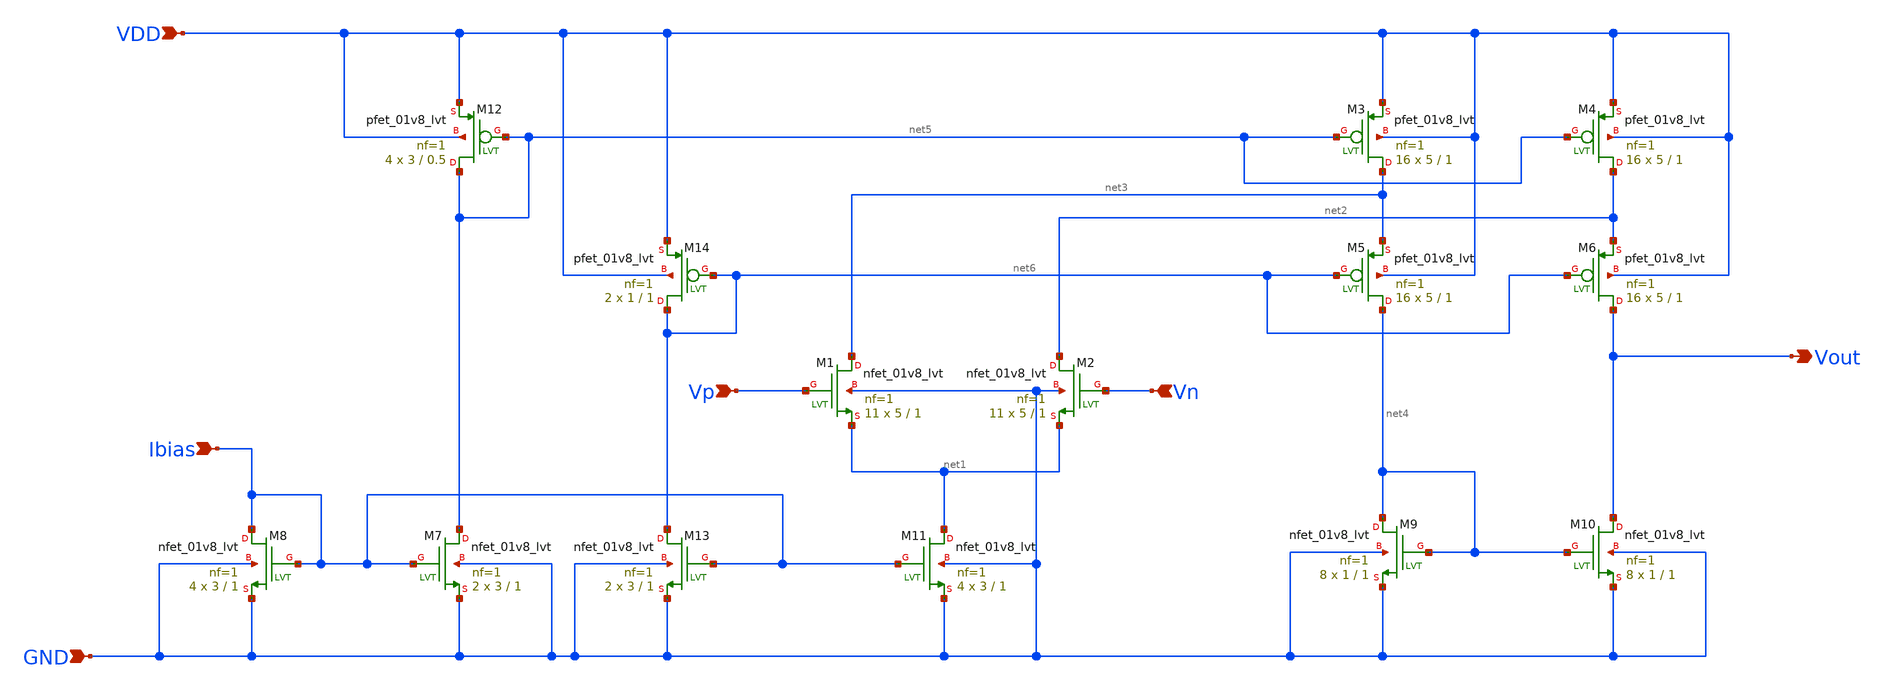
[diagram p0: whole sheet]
** sch_path: Analog_blocks/Analog_Blocks/OTA/Schematic/Folded_Cascode_OTA/Transistor1.8v/Folded_Cascode_OTA.sch
**.subckt Folded_Cascode_OTA VDD GND Vp Vn Vout Ibias
*.ipin VDD
*.ipin GND
*.ipin Vp
*.ipin Vn
*.opin Vout
*.ipin Ibias
XM1 net3 Vp net1 GND sky130_fd_pr__nfet_01v8_lvt L=1 W=5 nf=1 ad='int((nf+1)/2) * W/nf * 0.29' as='int((nf+2)/2) * W/nf * 0.29'
+ pd='2*int((nf+1)/2) * (W/nf + 0.29)' ps='2*int((nf+2)/2) * (W/nf + 0.29)' nrd='0.29 / W' nrs='0.29 / W'
+ sa=0 sb=0 sd=0 mult=11 m=11
XM2 net2 Vn net1 GND sky130_fd_pr__nfet_01v8_lvt L=1 W=5 nf=1 ad='int((nf+1)/2) * W/nf * 0.29' as='int((nf+2)/2) * W/nf * 0.29'
+ pd='2*int((nf+1)/2) * (W/nf + 0.29)' ps='2*int((nf+2)/2) * (W/nf + 0.29)' nrd='0.29 / W' nrs='0.29 / W'
+ sa=0 sb=0 sd=0 mult=11 m=11
XM3 net3 net5 VDD VDD sky130_fd_pr__pfet_01v8_lvt L=1 W=5 nf=1 ad='int((nf+1)/2) * W/nf * 0.29' as='int((nf+2)/2) * W/nf * 0.29'
+ pd='2*int((nf+1)/2) * (W/nf + 0.29)' ps='2*int((nf+2)/2) * (W/nf + 0.29)' nrd='0.29 / W' nrs='0.29 / W'
+ sa=0 sb=0 sd=0 mult=16 m=16
XM9 net4 net4 GND GND sky130_fd_pr__nfet_01v8_lvt L=1 W=1 nf=1 ad='int((nf+1)/2) * W/nf * 0.29' as='int((nf+2)/2) * W/nf * 0.29'
+ pd='2*int((nf+1)/2) * (W/nf + 0.29)' ps='2*int((nf+2)/2) * (W/nf + 0.29)' nrd='0.29 / W' nrs='0.29 / W'
+ sa=0 sb=0 sd=0 mult=8 m=8
XM10 Vout net4 GND GND sky130_fd_pr__nfet_01v8_lvt L=1 W=1 nf=1 ad='int((nf+1)/2) * W/nf * 0.29' as='int((nf+2)/2) * W/nf * 0.29'
+ pd='2*int((nf+1)/2) * (W/nf + 0.29)' ps='2*int((nf+2)/2) * (W/nf + 0.29)' nrd='0.29 / W' nrs='0.29 / W'
+ sa=0 sb=0 sd=0 mult=8 m=8
XM11 net1 Ibias GND GND sky130_fd_pr__nfet_01v8_lvt L=1 W=3 nf=1 ad='int((nf+1)/2) * W/nf * 0.29' as='int((nf+2)/2) * W/nf * 0.29'
+ pd='2*int((nf+1)/2) * (W/nf + 0.29)' ps='2*int((nf+2)/2) * (W/nf + 0.29)' nrd='0.29 / W' nrs='0.29 / W'
+ sa=0 sb=0 sd=0 mult=4 m=4
XM7 net5 Ibias GND GND sky130_fd_pr__nfet_01v8_lvt L=1 W=3 nf=1 ad='int((nf+1)/2) * W/nf * 0.29' as='int((nf+2)/2) * W/nf * 0.29'
+ pd='2*int((nf+1)/2) * (W/nf + 0.29)' ps='2*int((nf+2)/2) * (W/nf + 0.29)' nrd='0.29 / W' nrs='0.29 / W'
+ sa=0 sb=0 sd=0 mult=2 m=2
XM8 Ibias Ibias GND GND sky130_fd_pr__nfet_01v8_lvt L=1 W=3 nf=1 ad='int((nf+1)/2) * W/nf * 0.29' as='int((nf+2)/2) * W/nf * 0.29'
+ pd='2*int((nf+1)/2) * (W/nf + 0.29)' ps='2*int((nf+2)/2) * (W/nf + 0.29)' nrd='0.29 / W' nrs='0.29 / W'
+ sa=0 sb=0 sd=0 mult=4 m=4
XM12 net5 net5 VDD VDD sky130_fd_pr__pfet_01v8_lvt L=0.5 W=3 nf=1 ad='int((nf+1)/2) * W/nf * 0.29' as='int((nf+2)/2) * W/nf * 0.29'
+ pd='2*int((nf+1)/2) * (W/nf + 0.29)' ps='2*int((nf+2)/2) * (W/nf + 0.29)' nrd='0.29 / W' nrs='0.29 / W'
+ sa=0 sb=0 sd=0 mult=4 m=4
XM13 net6 Ibias GND GND sky130_fd_pr__nfet_01v8_lvt L=1 W=3 nf=1 ad='int((nf+1)/2) * W/nf * 0.29' as='int((nf+2)/2) * W/nf * 0.29'
+ pd='2*int((nf+1)/2) * (W/nf + 0.29)' ps='2*int((nf+2)/2) * (W/nf + 0.29)' nrd='0.29 / W' nrs='0.29 / W'
+ sa=0 sb=0 sd=0 mult=2 m=2
XM14 net6 net6 VDD VDD sky130_fd_pr__pfet_01v8_lvt L=1 W=1 nf=1 ad='int((nf+1)/2) * W/nf * 0.29' as='int((nf+2)/2) * W/nf * 0.29'
+ pd='2*int((nf+1)/2) * (W/nf + 0.29)' ps='2*int((nf+2)/2) * (W/nf + 0.29)' nrd='0.29 / W' nrs='0.29 / W'
+ sa=0 sb=0 sd=0 mult=2 m=2
XM4 net2 net5 VDD VDD sky130_fd_pr__pfet_01v8_lvt L=1 W=5 nf=1 ad='int((nf+1)/2) * W/nf * 0.29' as='int((nf+2)/2) * W/nf * 0.29'
+ pd='2*int((nf+1)/2) * (W/nf + 0.29)' ps='2*int((nf+2)/2) * (W/nf + 0.29)' nrd='0.29 / W' nrs='0.29 / W'
+ sa=0 sb=0 sd=0 mult=16 m=16
XM5 net4 net6 net3 VDD sky130_fd_pr__pfet_01v8_lvt L=1 W=5 nf=1 ad='int((nf+1)/2) * W/nf * 0.29' as='int((nf+2)/2) * W/nf * 0.29'
+ pd='2*int((nf+1)/2) * (W/nf + 0.29)' ps='2*int((nf+2)/2) * (W/nf + 0.29)' nrd='0.29 / W' nrs='0.29 / W'
+ sa=0 sb=0 sd=0 mult=16 m=16
XM6 Vout net6 net2 VDD sky130_fd_pr__pfet_01v8_lvt L=1 W=5 nf=1 ad='int((nf+1)/2) * W/nf * 0.29' as='int((nf+2)/2) * W/nf * 0.29'
+ pd='2*int((nf+1)/2) * (W/nf + 0.29)' ps='2*int((nf+2)/2) * (W/nf + 0.29)' nrd='0.29 / W' nrs='0.29 / W'
+ sa=0 sb=0 sd=0 mult=16 m=16
**.ends
.end
